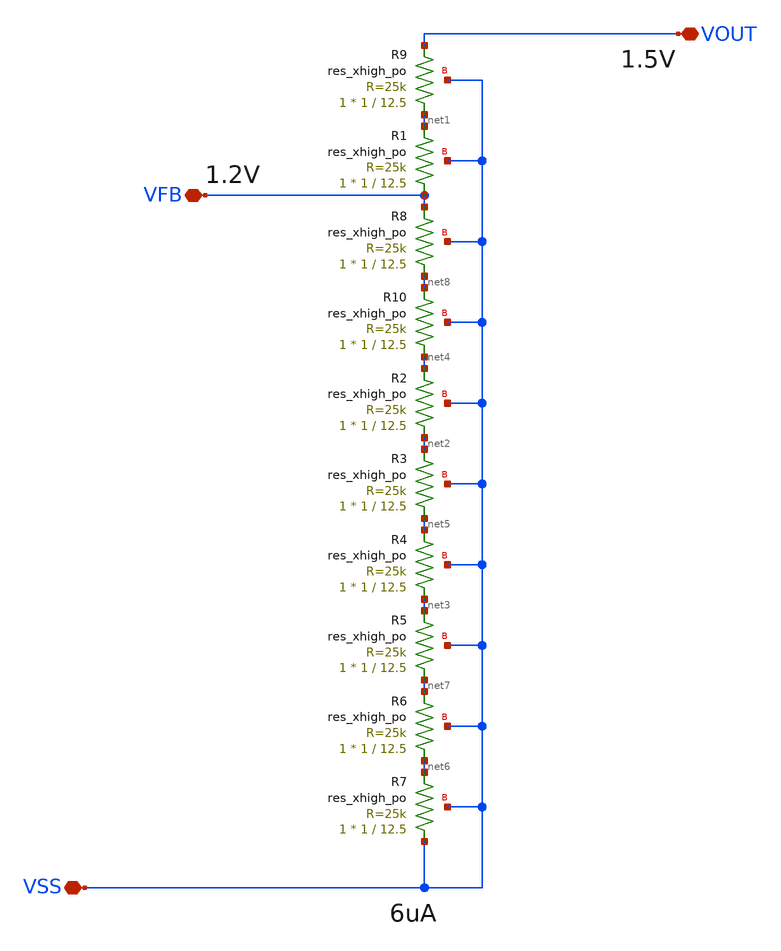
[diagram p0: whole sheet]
** sch_path: LDO_1p5V/schematics/RES_FB.sch
**.subckt RES_FB VOUT VFB VSS
*.iopin VOUT
*.iopin VFB
*.iopin VSS
XR9 net1 VOUT VSS sky130_fd_pr__res_xhigh_po W=1 L=12.5 mult=1 m=1
XR1 VFB net1 VSS sky130_fd_pr__res_xhigh_po W=1 L=12.5 mult=1 m=1
XR2 net2 net4 VSS sky130_fd_pr__res_xhigh_po W=1 L=12.5 mult=1 m=1
XR3 net5 net2 VSS sky130_fd_pr__res_xhigh_po W=1 L=12.5 mult=1 m=1
XR4 net3 net5 VSS sky130_fd_pr__res_xhigh_po W=1 L=12.5 mult=1 m=1
XR5 net7 net3 VSS sky130_fd_pr__res_xhigh_po W=1 L=12.5 mult=1 m=1
XR6 net6 net7 VSS sky130_fd_pr__res_xhigh_po W=1 L=12.5 mult=1 m=1
XR7 VSS net6 VSS sky130_fd_pr__res_xhigh_po W=1 L=12.5 mult=1 m=1
XR8 net8 VFB VSS sky130_fd_pr__res_xhigh_po W=1 L=12.5 mult=1 m=1
XR10 net4 net8 VSS sky130_fd_pr__res_xhigh_po W=1 L=12.5 mult=1 m=1
**.ends
.end
